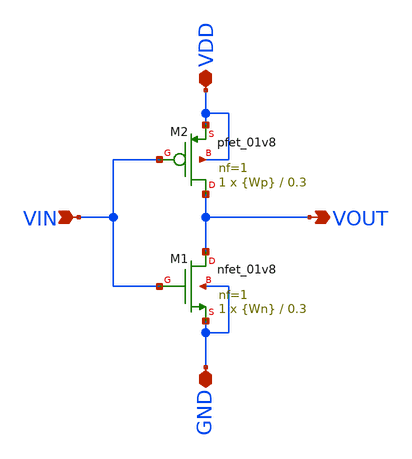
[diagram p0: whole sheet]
** sch_path: resuelto/schematic/inv.sch
**.subckt inv VDD GND VIN VOUT
*.iopin VDD
*.iopin GND
*.ipin VIN
*.opin VOUT
XM1 VOUT VIN GND GND sky130_fd_pr__nfet_01v8 L=0.3 W={Wn} nf=1 ad='int((nf+1)/2) * W/nf * 0.29' as='int((nf+2)/2) * W/nf * 0.29'
+ pd='2*int((nf+1)/2) * (W/nf + 0.29)' ps='2*int((nf+2)/2) * (W/nf + 0.29)' nrd='0.29 / W' nrs='0.29 / W'
+ sa=0 sb=0 sd=0 mult=1 m=1
XM2 VOUT VIN VDD VDD sky130_fd_pr__pfet_01v8 L=0.3 W={Wp} nf=1 ad='int((nf+1)/2) * W/nf * 0.29' as='int((nf+2)/2) * W/nf * 0.29'
+ pd='2*int((nf+1)/2) * (W/nf + 0.29)' ps='2*int((nf+2)/2) * (W/nf + 0.29)' nrd='0.29 / W' nrs='0.29 / W'
+ sa=0 sb=0 sd=0 mult=1 m=1
**.ends
.end
